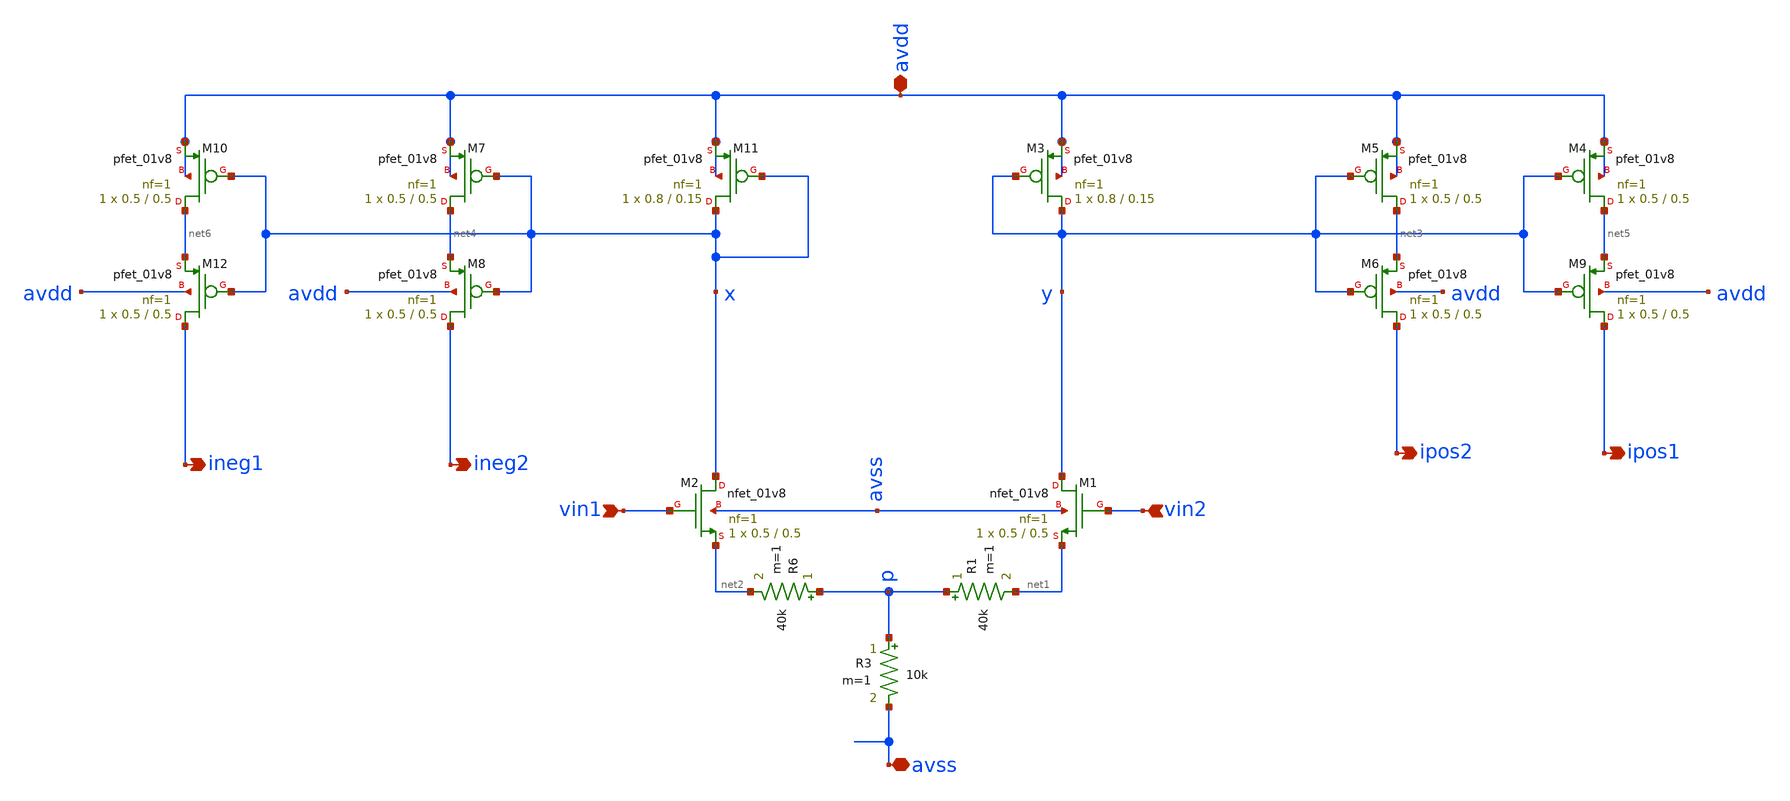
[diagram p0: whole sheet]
** sch_path: VCCS/otavccs4.sch
**.subckt otavccs4 avdd avss vin1 vin2 ineg2 ipos2 ipos1 ineg1
*.iopin avdd
*.iopin avss
*.ipin vin1
*.ipin vin2
*.opin ineg2
*.opin ipos2
*.opin ipos1
*.opin ineg1
XM2 x vin1 net2 avss sky130_fd_pr__nfet_01v8 L=0.5 W=0.5 nf=1 ad='int((1 + 1)/2) * 0.5 / 1 * 0.29' as='int((1 + 2)/2) * 0.5 / 1 * 0.29'
+ pd='2*int((1 + 1)/2) * (0.5 / 1 + 0.29)' ps='2*int((1 + 2)/2) * (0.5 / 1 + 0.29)' nrd='0.29 / 0.5 ' nrs='0.29 / 0.5 '
+ sa=0 sb=0 sd=0 mult=1 m=1
XM1 y vin2 net1 avss sky130_fd_pr__nfet_01v8 L=0.5 W=0.5 nf=1 ad='int((1 + 1)/2) * 0.5 / 1 * 0.29' as='int((1 + 2)/2) * 0.5 / 1 * 0.29'
+ pd='2*int((1 + 1)/2) * (0.5 / 1 + 0.29)' ps='2*int((1 + 2)/2) * (0.5 / 1 + 0.29)' nrd='0.29 / 0.5 ' nrs='0.29 / 0.5 '
+ sa=0 sb=0 sd=0 mult=1 m=1
XM11 x x avdd avdd sky130_fd_pr__pfet_01v8 L=0.15 W=0.8 nf=1 ad='int((nf+1)/2) * W/nf * 0.29' as='int((nf+2)/2) * W/nf * 0.29'
+ pd='2*int((nf+1)/2) * (W/nf + 0.29)' ps='2*int((nf+2)/2) * (W/nf + 0.29)' nrd='0.29 / W' nrs='0.29 / W'
+ sa=0 sb=0 sd=0 mult=1 m=1
XM3 y y avdd avdd sky130_fd_pr__pfet_01v8 L=0.15 W=0.8 nf=1 ad='int((nf+1)/2) * W/nf * 0.29' as='int((nf+2)/2) * W/nf * 0.29'
+ pd='2*int((nf+1)/2) * (W/nf + 0.29)' ps='2*int((nf+2)/2) * (W/nf + 0.29)' nrd='0.29 / W' nrs='0.29 / W'
+ sa=0 sb=0 sd=0 mult=1 m=1
XM5 net3 y avdd avdd sky130_fd_pr__pfet_01v8 L=0.5 W=0.5 nf=1 ad='int((nf+1)/2) * W/nf * 0.29' as='int((nf+2)/2) * W/nf * 0.29'
+ pd='2*int((nf+1)/2) * (W/nf + 0.29)' ps='2*int((nf+2)/2) * (W/nf + 0.29)' nrd='0.29 / W' nrs='0.29 / W'
+ sa=0 sb=0 sd=0 mult=1 m=1
XM6 ipos2 y net3 avdd sky130_fd_pr__pfet_01v8 L=0.5 W=0.5 nf=1 ad='int((nf+1)/2) * W/nf * 0.29' as='int((nf+2)/2) * W/nf * 0.29'
+ pd='2*int((nf+1)/2) * (W/nf + 0.29)' ps='2*int((nf+2)/2) * (W/nf + 0.29)' nrd='0.29 / W' nrs='0.29 / W'
+ sa=0 sb=0 sd=0 mult=1 m=1
XM7 net4 x avdd avdd sky130_fd_pr__pfet_01v8 L=0.5 W=0.5 nf=1 ad='int((nf+1)/2) * W/nf * 0.29' as='int((nf+2)/2) * W/nf * 0.29'
+ pd='2*int((nf+1)/2) * (W/nf + 0.29)' ps='2*int((nf+2)/2) * (W/nf + 0.29)' nrd='0.29 / W' nrs='0.29 / W'
+ sa=0 sb=0 sd=0 mult=1 m=1
XM8 ineg2 x net4 avdd sky130_fd_pr__pfet_01v8 L=0.5 W=0.5 nf=1 ad='int((nf+1)/2) * W/nf * 0.29' as='int((nf+2)/2) * W/nf * 0.29'
+ pd='2*int((nf+1)/2) * (W/nf + 0.29)' ps='2*int((nf+2)/2) * (W/nf + 0.29)' nrd='0.29 / W' nrs='0.29 / W'
+ sa=0 sb=0 sd=0 mult=1 m=1
R3 p avss 10k m=1
R6 p net2 40k m=1
R1 p net1 40k m=1
XM4 net5 y avdd avdd sky130_fd_pr__pfet_01v8 L=0.5 W=0.5 nf=1 ad='int((nf+1)/2) * W/nf * 0.29' as='int((nf+2)/2) * W/nf * 0.29'
+ pd='2*int((nf+1)/2) * (W/nf + 0.29)' ps='2*int((nf+2)/2) * (W/nf + 0.29)' nrd='0.29 / W' nrs='0.29 / W'
+ sa=0 sb=0 sd=0 mult=1 m=1
XM9 ipos1 y net5 avdd sky130_fd_pr__pfet_01v8 L=0.5 W=0.5 nf=1 ad='int((nf+1)/2) * W/nf * 0.29' as='int((nf+2)/2) * W/nf * 0.29'
+ pd='2*int((nf+1)/2) * (W/nf + 0.29)' ps='2*int((nf+2)/2) * (W/nf + 0.29)' nrd='0.29 / W' nrs='0.29 / W'
+ sa=0 sb=0 sd=0 mult=1 m=1
XM10 net6 x avdd avdd sky130_fd_pr__pfet_01v8 L=0.5 W=0.5 nf=1 ad='int((nf+1)/2) * W/nf * 0.29' as='int((nf+2)/2) * W/nf * 0.29'
+ pd='2*int((nf+1)/2) * (W/nf + 0.29)' ps='2*int((nf+2)/2) * (W/nf + 0.29)' nrd='0.29 / W' nrs='0.29 / W'
+ sa=0 sb=0 sd=0 mult=1 m=1
XM12 ineg1 x net6 avdd sky130_fd_pr__pfet_01v8 L=0.5 W=0.5 nf=1 ad='int((nf+1)/2) * W/nf * 0.29' as='int((nf+2)/2) * W/nf * 0.29'
+ pd='2*int((nf+1)/2) * (W/nf + 0.29)' ps='2*int((nf+2)/2) * (W/nf + 0.29)' nrd='0.29 / W' nrs='0.29 / W'
+ sa=0 sb=0 sd=0 mult=1 m=1
**.ends
.end
